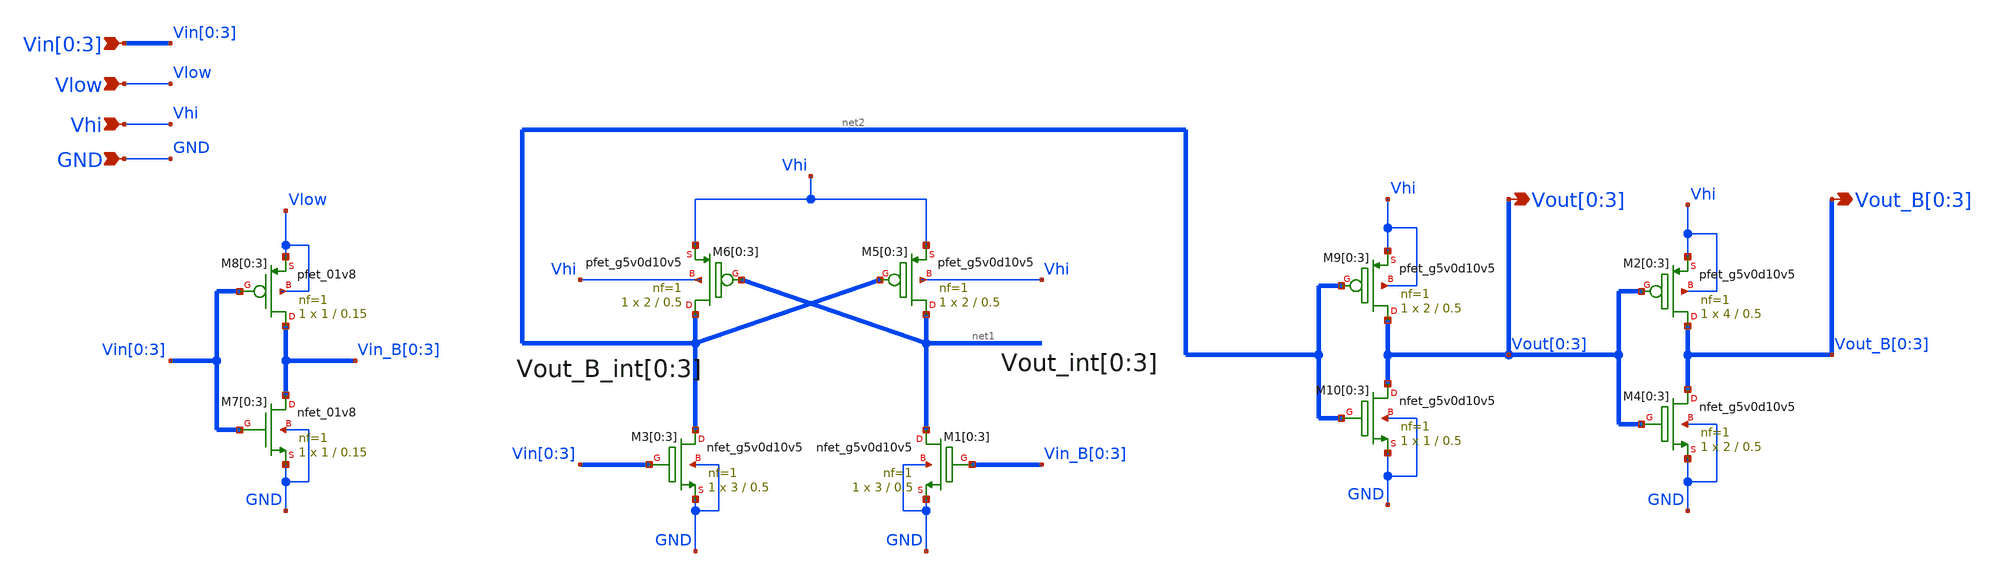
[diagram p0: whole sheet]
** sch_path: sky130_cells/Level_Shifter/Horizontal_LS/level_shifter_horizontal.sch
* Copyright 2021 Stefan Frederik Schippers
* Licensed under the Apache License, Version 2.0 (the "License");
* you may not use this file except in compliance with the License.
* You may obtain a copy of the License at
* https://www.apache.org/licenses/LICENSE-2.0
* Unless required by applicable law or agreed to in writing, software
* distributed under the License is distributed on an "AS IS" BASIS,
* WITHOUT WARRANTIES OR CONDITIONS OF ANY KIND, either express or implied.
* See the License for the specific language governing permissions and
* limitations under the License.
**.subckt level_shifter_horizontal Vlow Vhi Vin[0],Vin[1],Vin[2],Vin[3]
*+ Vout[0],Vout[1],Vout[2],Vout[3] GND Vout_B[0],Vout_B[1],Vout_B[2],Vout_B[3]
*.ipin Vlow
*.ipin Vhi
*.ipin Vin[0],Vin[1],Vin[2],Vin[3]
*.opin Vout[0],Vout[1],Vout[2],Vout[3]
*.ipin GND
*.opin Vout_B[0],Vout_B[1],Vout_B[2],Vout_B[3]
XM5[0] net1[3] net2[3] Vhi Vhi sky130_fd_pr__pfet_g5v0d10v5 L=0.5 W=2 nf=1 ad='int((nf+1)/2) * W/nf * 0.29'
+ as='int((nf+2)/2) * W/nf * 0.29' pd='2*int((nf+1)/2) * (W/nf + 0.29)' ps='2*int((nf+2)/2) * (W/nf + 0.29)'
+ nrd='0.29 / W' nrs='0.29 / W' sa=0 sb=0 sd=0 mult=1 m=1
XM5[1] net1[2] net2[2] Vhi Vhi sky130_fd_pr__pfet_g5v0d10v5 L=0.5 W=2 nf=1 ad='int((nf+1)/2) * W/nf * 0.29'
+ as='int((nf+2)/2) * W/nf * 0.29' pd='2*int((nf+1)/2) * (W/nf + 0.29)' ps='2*int((nf+2)/2) * (W/nf + 0.29)'
+ nrd='0.29 / W' nrs='0.29 / W' sa=0 sb=0 sd=0 mult=1 m=1
XM5[2] net1[1] net2[1] Vhi Vhi sky130_fd_pr__pfet_g5v0d10v5 L=0.5 W=2 nf=1 ad='int((nf+1)/2) * W/nf * 0.29'
+ as='int((nf+2)/2) * W/nf * 0.29' pd='2*int((nf+1)/2) * (W/nf + 0.29)' ps='2*int((nf+2)/2) * (W/nf + 0.29)'
+ nrd='0.29 / W' nrs='0.29 / W' sa=0 sb=0 sd=0 mult=1 m=1
XM5[3] net1[0] net2[0] Vhi Vhi sky130_fd_pr__pfet_g5v0d10v5 L=0.5 W=2 nf=1 ad='int((nf+1)/2) * W/nf * 0.29'
+ as='int((nf+2)/2) * W/nf * 0.29' pd='2*int((nf+1)/2) * (W/nf + 0.29)' ps='2*int((nf+2)/2) * (W/nf + 0.29)'
+ nrd='0.29 / W' nrs='0.29 / W' sa=0 sb=0 sd=0 mult=1 m=1
XM6[0] net2[3] net1[3] Vhi Vhi sky130_fd_pr__pfet_g5v0d10v5 L=0.5 W=2 nf=1 ad='int((nf+1)/2) * W/nf * 0.29'
+ as='int((nf+2)/2) * W/nf * 0.29' pd='2*int((nf+1)/2) * (W/nf + 0.29)' ps='2*int((nf+2)/2) * (W/nf + 0.29)'
+ nrd='0.29 / W' nrs='0.29 / W' sa=0 sb=0 sd=0 mult=1 m=1
XM6[1] net2[2] net1[2] Vhi Vhi sky130_fd_pr__pfet_g5v0d10v5 L=0.5 W=2 nf=1 ad='int((nf+1)/2) * W/nf * 0.29'
+ as='int((nf+2)/2) * W/nf * 0.29' pd='2*int((nf+1)/2) * (W/nf + 0.29)' ps='2*int((nf+2)/2) * (W/nf + 0.29)'
+ nrd='0.29 / W' nrs='0.29 / W' sa=0 sb=0 sd=0 mult=1 m=1
XM6[2] net2[1] net1[1] Vhi Vhi sky130_fd_pr__pfet_g5v0d10v5 L=0.5 W=2 nf=1 ad='int((nf+1)/2) * W/nf * 0.29'
+ as='int((nf+2)/2) * W/nf * 0.29' pd='2*int((nf+1)/2) * (W/nf + 0.29)' ps='2*int((nf+2)/2) * (W/nf + 0.29)'
+ nrd='0.29 / W' nrs='0.29 / W' sa=0 sb=0 sd=0 mult=1 m=1
XM6[3] net2[0] net1[0] Vhi Vhi sky130_fd_pr__pfet_g5v0d10v5 L=0.5 W=2 nf=1 ad='int((nf+1)/2) * W/nf * 0.29'
+ as='int((nf+2)/2) * W/nf * 0.29' pd='2*int((nf+1)/2) * (W/nf + 0.29)' ps='2*int((nf+2)/2) * (W/nf + 0.29)'
+ nrd='0.29 / W' nrs='0.29 / W' sa=0 sb=0 sd=0 mult=1 m=1
XM7[0] Vin_B[0] Vin[0] GND GND sky130_fd_pr__nfet_01v8 L=0.15 W=1 nf=1 ad='int((nf+1)/2) * W/nf * 0.29'
+ as='int((nf+2)/2) * W/nf * 0.29' pd='2*int((nf+1)/2) * (W/nf + 0.29)' ps='2*int((nf+2)/2) * (W/nf + 0.29)'
+ nrd='0.29 / W' nrs='0.29 / W' sa=0 sb=0 sd=0 mult=1 m=1
XM7[1] Vin_B[1] Vin[1] GND GND sky130_fd_pr__nfet_01v8 L=0.15 W=1 nf=1 ad='int((nf+1)/2) * W/nf * 0.29'
+ as='int((nf+2)/2) * W/nf * 0.29' pd='2*int((nf+1)/2) * (W/nf + 0.29)' ps='2*int((nf+2)/2) * (W/nf + 0.29)'
+ nrd='0.29 / W' nrs='0.29 / W' sa=0 sb=0 sd=0 mult=1 m=1
XM7[2] Vin_B[2] Vin[2] GND GND sky130_fd_pr__nfet_01v8 L=0.15 W=1 nf=1 ad='int((nf+1)/2) * W/nf * 0.29'
+ as='int((nf+2)/2) * W/nf * 0.29' pd='2*int((nf+1)/2) * (W/nf + 0.29)' ps='2*int((nf+2)/2) * (W/nf + 0.29)'
+ nrd='0.29 / W' nrs='0.29 / W' sa=0 sb=0 sd=0 mult=1 m=1
XM7[3] Vin_B[3] Vin[3] GND GND sky130_fd_pr__nfet_01v8 L=0.15 W=1 nf=1 ad='int((nf+1)/2) * W/nf * 0.29'
+ as='int((nf+2)/2) * W/nf * 0.29' pd='2*int((nf+1)/2) * (W/nf + 0.29)' ps='2*int((nf+2)/2) * (W/nf + 0.29)'
+ nrd='0.29 / W' nrs='0.29 / W' sa=0 sb=0 sd=0 mult=1 m=1
XM8[0] Vin_B[0] Vin[0] Vlow Vlow sky130_fd_pr__pfet_01v8 L=0.15 W=1 nf=1 ad='int((nf+1)/2) * W/nf * 0.29'
+ as='int((nf+2)/2) * W/nf * 0.29' pd='2*int((nf+1)/2) * (W/nf + 0.29)' ps='2*int((nf+2)/2) * (W/nf + 0.29)'
+ nrd='0.29 / W' nrs='0.29 / W' sa=0 sb=0 sd=0 mult=1 m=1
XM8[1] Vin_B[1] Vin[1] Vlow Vlow sky130_fd_pr__pfet_01v8 L=0.15 W=1 nf=1 ad='int((nf+1)/2) * W/nf * 0.29'
+ as='int((nf+2)/2) * W/nf * 0.29' pd='2*int((nf+1)/2) * (W/nf + 0.29)' ps='2*int((nf+2)/2) * (W/nf + 0.29)'
+ nrd='0.29 / W' nrs='0.29 / W' sa=0 sb=0 sd=0 mult=1 m=1
XM8[2] Vin_B[2] Vin[2] Vlow Vlow sky130_fd_pr__pfet_01v8 L=0.15 W=1 nf=1 ad='int((nf+1)/2) * W/nf * 0.29'
+ as='int((nf+2)/2) * W/nf * 0.29' pd='2*int((nf+1)/2) * (W/nf + 0.29)' ps='2*int((nf+2)/2) * (W/nf + 0.29)'
+ nrd='0.29 / W' nrs='0.29 / W' sa=0 sb=0 sd=0 mult=1 m=1
XM8[3] Vin_B[3] Vin[3] Vlow Vlow sky130_fd_pr__pfet_01v8 L=0.15 W=1 nf=1 ad='int((nf+1)/2) * W/nf * 0.29'
+ as='int((nf+2)/2) * W/nf * 0.29' pd='2*int((nf+1)/2) * (W/nf + 0.29)' ps='2*int((nf+2)/2) * (W/nf + 0.29)'
+ nrd='0.29 / W' nrs='0.29 / W' sa=0 sb=0 sd=0 mult=1 m=1
XM9[0] Vout[0] net2[3] Vhi Vhi sky130_fd_pr__pfet_g5v0d10v5 L=0.5 W=2 nf=1 ad='int((nf+1)/2) * W/nf * 0.29'
+ as='int((nf+2)/2) * W/nf * 0.29' pd='2*int((nf+1)/2) * (W/nf + 0.29)' ps='2*int((nf+2)/2) * (W/nf + 0.29)'
+ nrd='0.29 / W' nrs='0.29 / W' sa=0 sb=0 sd=0 mult=1 m=1
XM9[1] Vout[1] net2[2] Vhi Vhi sky130_fd_pr__pfet_g5v0d10v5 L=0.5 W=2 nf=1 ad='int((nf+1)/2) * W/nf * 0.29'
+ as='int((nf+2)/2) * W/nf * 0.29' pd='2*int((nf+1)/2) * (W/nf + 0.29)' ps='2*int((nf+2)/2) * (W/nf + 0.29)'
+ nrd='0.29 / W' nrs='0.29 / W' sa=0 sb=0 sd=0 mult=1 m=1
XM9[2] Vout[2] net2[1] Vhi Vhi sky130_fd_pr__pfet_g5v0d10v5 L=0.5 W=2 nf=1 ad='int((nf+1)/2) * W/nf * 0.29'
+ as='int((nf+2)/2) * W/nf * 0.29' pd='2*int((nf+1)/2) * (W/nf + 0.29)' ps='2*int((nf+2)/2) * (W/nf + 0.29)'
+ nrd='0.29 / W' nrs='0.29 / W' sa=0 sb=0 sd=0 mult=1 m=1
XM9[3] Vout[3] net2[0] Vhi Vhi sky130_fd_pr__pfet_g5v0d10v5 L=0.5 W=2 nf=1 ad='int((nf+1)/2) * W/nf * 0.29'
+ as='int((nf+2)/2) * W/nf * 0.29' pd='2*int((nf+1)/2) * (W/nf + 0.29)' ps='2*int((nf+2)/2) * (W/nf + 0.29)'
+ nrd='0.29 / W' nrs='0.29 / W' sa=0 sb=0 sd=0 mult=1 m=1
XM10[0] Vout[0] net2[3] GND GND sky130_fd_pr__nfet_g5v0d10v5 L=0.5 W=1 nf=1 ad='int((nf+1)/2) * W/nf * 0.29'
+ as='int((nf+2)/2) * W/nf * 0.29' pd='2*int((nf+1)/2) * (W/nf + 0.29)' ps='2*int((nf+2)/2) * (W/nf + 0.29)'
+ nrd='0.29 / W' nrs='0.29 / W' sa=0 sb=0 sd=0 mult=1 m=1
XM10[1] Vout[1] net2[2] GND GND sky130_fd_pr__nfet_g5v0d10v5 L=0.5 W=1 nf=1 ad='int((nf+1)/2) * W/nf * 0.29'
+ as='int((nf+2)/2) * W/nf * 0.29' pd='2*int((nf+1)/2) * (W/nf + 0.29)' ps='2*int((nf+2)/2) * (W/nf + 0.29)'
+ nrd='0.29 / W' nrs='0.29 / W' sa=0 sb=0 sd=0 mult=1 m=1
XM10[2] Vout[2] net2[1] GND GND sky130_fd_pr__nfet_g5v0d10v5 L=0.5 W=1 nf=1 ad='int((nf+1)/2) * W/nf * 0.29'
+ as='int((nf+2)/2) * W/nf * 0.29' pd='2*int((nf+1)/2) * (W/nf + 0.29)' ps='2*int((nf+2)/2) * (W/nf + 0.29)'
+ nrd='0.29 / W' nrs='0.29 / W' sa=0 sb=0 sd=0 mult=1 m=1
XM10[3] Vout[3] net2[0] GND GND sky130_fd_pr__nfet_g5v0d10v5 L=0.5 W=1 nf=1 ad='int((nf+1)/2) * W/nf * 0.29'
+ as='int((nf+2)/2) * W/nf * 0.29' pd='2*int((nf+1)/2) * (W/nf + 0.29)' ps='2*int((nf+2)/2) * (W/nf + 0.29)'
+ nrd='0.29 / W' nrs='0.29 / W' sa=0 sb=0 sd=0 mult=1 m=1
XM3[0] net2[3] Vin[0] GND GND sky130_fd_pr__nfet_g5v0d10v5 L=0.5 W=3 nf=1 ad='int((nf+1)/2) * W/nf * 0.29'
+ as='int((nf+2)/2) * W/nf * 0.29' pd='2*int((nf+1)/2) * (W/nf + 0.29)' ps='2*int((nf+2)/2) * (W/nf + 0.29)'
+ nrd='0.29 / W' nrs='0.29 / W' sa=0 sb=0 sd=0 mult=1 m=1
XM3[1] net2[2] Vin[1] GND GND sky130_fd_pr__nfet_g5v0d10v5 L=0.5 W=3 nf=1 ad='int((nf+1)/2) * W/nf * 0.29'
+ as='int((nf+2)/2) * W/nf * 0.29' pd='2*int((nf+1)/2) * (W/nf + 0.29)' ps='2*int((nf+2)/2) * (W/nf + 0.29)'
+ nrd='0.29 / W' nrs='0.29 / W' sa=0 sb=0 sd=0 mult=1 m=1
XM3[2] net2[1] Vin[2] GND GND sky130_fd_pr__nfet_g5v0d10v5 L=0.5 W=3 nf=1 ad='int((nf+1)/2) * W/nf * 0.29'
+ as='int((nf+2)/2) * W/nf * 0.29' pd='2*int((nf+1)/2) * (W/nf + 0.29)' ps='2*int((nf+2)/2) * (W/nf + 0.29)'
+ nrd='0.29 / W' nrs='0.29 / W' sa=0 sb=0 sd=0 mult=1 m=1
XM3[3] net2[0] Vin[3] GND GND sky130_fd_pr__nfet_g5v0d10v5 L=0.5 W=3 nf=1 ad='int((nf+1)/2) * W/nf * 0.29'
+ as='int((nf+2)/2) * W/nf * 0.29' pd='2*int((nf+1)/2) * (W/nf + 0.29)' ps='2*int((nf+2)/2) * (W/nf + 0.29)'
+ nrd='0.29 / W' nrs='0.29 / W' sa=0 sb=0 sd=0 mult=1 m=1
XM1[0] net1[3] Vin_B[0] GND GND sky130_fd_pr__nfet_g5v0d10v5 L=0.5 W=3 nf=1 ad='int((nf+1)/2) * W/nf * 0.29'
+ as='int((nf+2)/2) * W/nf * 0.29' pd='2*int((nf+1)/2) * (W/nf + 0.29)' ps='2*int((nf+2)/2) * (W/nf + 0.29)'
+ nrd='0.29 / W' nrs='0.29 / W' sa=0 sb=0 sd=0 mult=1 m=1
XM1[1] net1[2] Vin_B[1] GND GND sky130_fd_pr__nfet_g5v0d10v5 L=0.5 W=3 nf=1 ad='int((nf+1)/2) * W/nf * 0.29'
+ as='int((nf+2)/2) * W/nf * 0.29' pd='2*int((nf+1)/2) * (W/nf + 0.29)' ps='2*int((nf+2)/2) * (W/nf + 0.29)'
+ nrd='0.29 / W' nrs='0.29 / W' sa=0 sb=0 sd=0 mult=1 m=1
XM1[2] net1[1] Vin_B[2] GND GND sky130_fd_pr__nfet_g5v0d10v5 L=0.5 W=3 nf=1 ad='int((nf+1)/2) * W/nf * 0.29'
+ as='int((nf+2)/2) * W/nf * 0.29' pd='2*int((nf+1)/2) * (W/nf + 0.29)' ps='2*int((nf+2)/2) * (W/nf + 0.29)'
+ nrd='0.29 / W' nrs='0.29 / W' sa=0 sb=0 sd=0 mult=1 m=1
XM1[3] net1[0] Vin_B[3] GND GND sky130_fd_pr__nfet_g5v0d10v5 L=0.5 W=3 nf=1 ad='int((nf+1)/2) * W/nf * 0.29'
+ as='int((nf+2)/2) * W/nf * 0.29' pd='2*int((nf+1)/2) * (W/nf + 0.29)' ps='2*int((nf+2)/2) * (W/nf + 0.29)'
+ nrd='0.29 / W' nrs='0.29 / W' sa=0 sb=0 sd=0 mult=1 m=1
XM2[0] Vout_B[0] Vout[0] Vhi Vhi sky130_fd_pr__pfet_g5v0d10v5 L=0.5 W=4 nf=1 ad='int((nf+1)/2) * W/nf * 0.29'
+ as='int((nf+2)/2) * W/nf * 0.29' pd='2*int((nf+1)/2) * (W/nf + 0.29)' ps='2*int((nf+2)/2) * (W/nf + 0.29)'
+ nrd='0.29 / W' nrs='0.29 / W' sa=0 sb=0 sd=0 mult=1 m=1
XM2[1] Vout_B[1] Vout[1] Vhi Vhi sky130_fd_pr__pfet_g5v0d10v5 L=0.5 W=4 nf=1 ad='int((nf+1)/2) * W/nf * 0.29'
+ as='int((nf+2)/2) * W/nf * 0.29' pd='2*int((nf+1)/2) * (W/nf + 0.29)' ps='2*int((nf+2)/2) * (W/nf + 0.29)'
+ nrd='0.29 / W' nrs='0.29 / W' sa=0 sb=0 sd=0 mult=1 m=1
XM2[2] Vout_B[2] Vout[2] Vhi Vhi sky130_fd_pr__pfet_g5v0d10v5 L=0.5 W=4 nf=1 ad='int((nf+1)/2) * W/nf * 0.29'
+ as='int((nf+2)/2) * W/nf * 0.29' pd='2*int((nf+1)/2) * (W/nf + 0.29)' ps='2*int((nf+2)/2) * (W/nf + 0.29)'
+ nrd='0.29 / W' nrs='0.29 / W' sa=0 sb=0 sd=0 mult=1 m=1
XM2[3] Vout_B[3] Vout[3] Vhi Vhi sky130_fd_pr__pfet_g5v0d10v5 L=0.5 W=4 nf=1 ad='int((nf+1)/2) * W/nf * 0.29'
+ as='int((nf+2)/2) * W/nf * 0.29' pd='2*int((nf+1)/2) * (W/nf + 0.29)' ps='2*int((nf+2)/2) * (W/nf + 0.29)'
+ nrd='0.29 / W' nrs='0.29 / W' sa=0 sb=0 sd=0 mult=1 m=1
XM4[0] Vout_B[0] Vout[0] GND GND sky130_fd_pr__nfet_g5v0d10v5 L=0.5 W=2 nf=1 ad='int((nf+1)/2) * W/nf * 0.29'
+ as='int((nf+2)/2) * W/nf * 0.29' pd='2*int((nf+1)/2) * (W/nf + 0.29)' ps='2*int((nf+2)/2) * (W/nf + 0.29)'
+ nrd='0.29 / W' nrs='0.29 / W' sa=0 sb=0 sd=0 mult=1 m=1
XM4[1] Vout_B[1] Vout[1] GND GND sky130_fd_pr__nfet_g5v0d10v5 L=0.5 W=2 nf=1 ad='int((nf+1)/2) * W/nf * 0.29'
+ as='int((nf+2)/2) * W/nf * 0.29' pd='2*int((nf+1)/2) * (W/nf + 0.29)' ps='2*int((nf+2)/2) * (W/nf + 0.29)'
+ nrd='0.29 / W' nrs='0.29 / W' sa=0 sb=0 sd=0 mult=1 m=1
XM4[2] Vout_B[2] Vout[2] GND GND sky130_fd_pr__nfet_g5v0d10v5 L=0.5 W=2 nf=1 ad='int((nf+1)/2) * W/nf * 0.29'
+ as='int((nf+2)/2) * W/nf * 0.29' pd='2*int((nf+1)/2) * (W/nf + 0.29)' ps='2*int((nf+2)/2) * (W/nf + 0.29)'
+ nrd='0.29 / W' nrs='0.29 / W' sa=0 sb=0 sd=0 mult=1 m=1
XM4[3] Vout_B[3] Vout[3] GND GND sky130_fd_pr__nfet_g5v0d10v5 L=0.5 W=2 nf=1 ad='int((nf+1)/2) * W/nf * 0.29'
+ as='int((nf+2)/2) * W/nf * 0.29' pd='2*int((nf+1)/2) * (W/nf + 0.29)' ps='2*int((nf+2)/2) * (W/nf + 0.29)'
+ nrd='0.29 / W' nrs='0.29 / W' sa=0 sb=0 sd=0 mult=1 m=1
**.ends
.end
